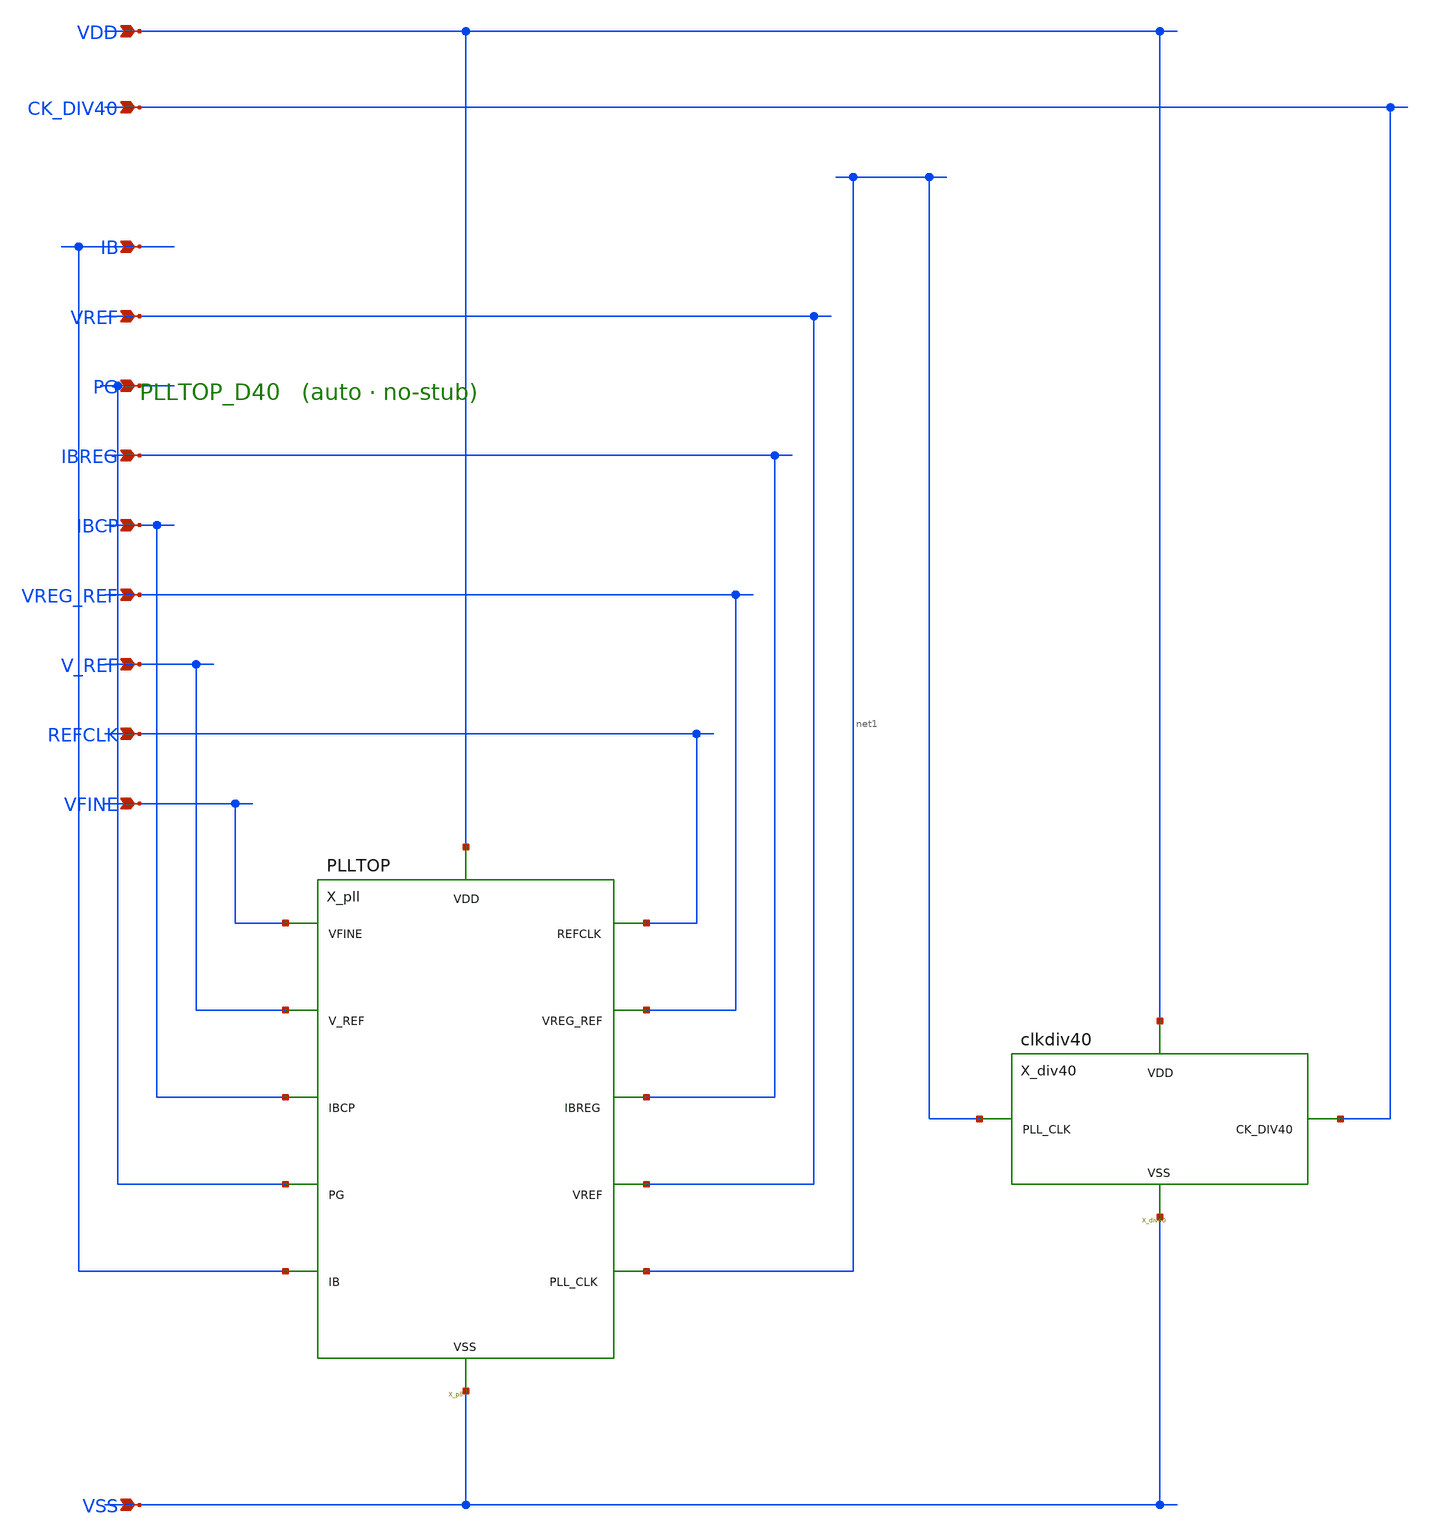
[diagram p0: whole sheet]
** sch_path: schematics/PLLTOP_D40.sch
**.subckt PLLTOP_D40 VDD VSS VFINE REFCLK V_REF VREG_REF IBCP IBREG PG VREF IB CK_DIV40
*.ipin VDD
*.ipin VSS
*.ipin VFINE
*.ipin REFCLK
*.ipin V_REF
*.ipin VREG_REF
*.ipin IBCP
*.ipin IBREG
*.ipin PG
*.ipin VREF
*.ipin IB
*.ipin CK_DIV40
X_pll VDD VSS VFINE REFCLK V_REF VREG_REF IBCP IBREG PG VREF IB net1 PLLTOP
X_div40 net1 VDD VSS CK_DIV40 clkdiv40
**.ends
.end
